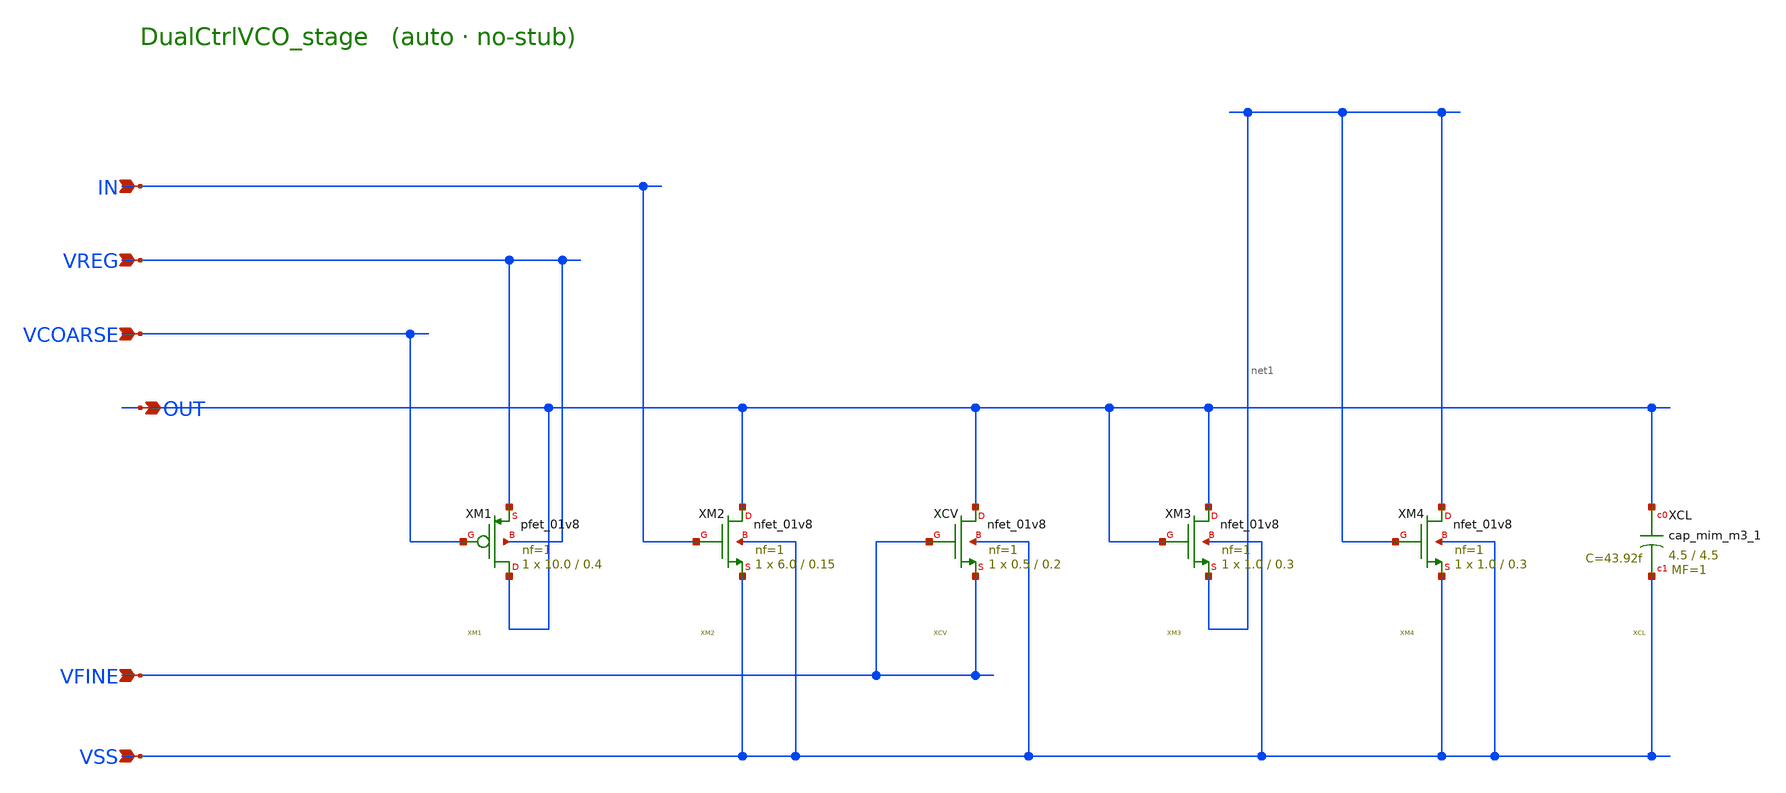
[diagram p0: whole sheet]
** sch_path: schematics/DualCtrlVCO_stage.sch
**.subckt DualCtrlVCO_stage IN OUT VCOARSE VFINE VREG VSS
*.ipin IN
*.opin OUT
*.ipin VCOARSE
*.ipin VFINE
*.ipin VREG
*.ipin VSS
XXM1 OUT VCOARSE VREG VREG sky130_fd_pr__pfet_01v8 L=0.4 W=10.0 nf=1 ad='int((nf+1)/2) * W/nf * 0.29'
+ as='int((nf+2)/2) * W/nf * 0.29' pd='2*int((nf+1)/2) * (W/nf + 0.29)' ps='2*int((nf+2)/2) * (W/nf + 0.29)'
+ nrd='0.29 / W' nrs='0.29 / W' sa=0 sb=0 sd=0 mult=1 m=1
XXM2 OUT IN VSS VSS sky130_fd_pr__nfet_01v8 L=0.15 W=6.0 nf=1 ad='int((1 + 1)/2) * 6.0 / 1 * 0.29' as='int((1 + 2)/2) * 6.0 / 1 * 0.29'
+ pd='2*int((1 + 1)/2) * (6.0 / 1 + 0.29)' ps='2*int((1 + 2)/2) * (6.0 / 1 + 0.29)' nrd='0.29 / 6.0 ' nrs='0.29 / 6.0 '
+ sa=0 sb=0 sd=0 mult=1 m=1
XXCV OUT VFINE VFINE VSS sky130_fd_pr__nfet_01v8 L=0.2 W=0.5 nf=1 ad='int((1 + 1)/2) * 0.5 / 1 * 0.29'
+ as='int((1 + 2)/2) * 0.5 / 1 * 0.29' pd='2*int((1 + 1)/2) * (0.5 / 1 + 0.29)' ps='2*int((1 + 2)/2) * (0.5 / 1 + 0.29)'
+ nrd='0.29 / 0.5 ' nrs='0.29 / 0.5 ' sa=0 sb=0 sd=0 mult=1 m=1
XXM3 OUT OUT net1 VSS sky130_fd_pr__nfet_01v8 L=0.3 W=1.0 nf=1 ad='int((1 + 1)/2) * 1.0 / 1 * 0.29' as='int((1 + 2)/2) * 1.0 / 1 * 0.29'
+ pd='2*int((1 + 1)/2) * (1.0 / 1 + 0.29)' ps='2*int((1 + 2)/2) * (1.0 / 1 + 0.29)' nrd='0.29 / 1.0 ' nrs='0.29 / 1.0 '
+ sa=0 sb=0 sd=0 mult=1 m=1
XXM4 net1 net1 VSS VSS sky130_fd_pr__nfet_01v8 L=0.3 W=1.0 nf=1 ad='int((1 + 1)/2) * 1.0 / 1 * 0.29'
+ as='int((1 + 2)/2) * 1.0 / 1 * 0.29' pd='2*int((1 + 1)/2) * (1.0 / 1 + 0.29)' ps='2*int((1 + 2)/2) * (1.0 / 1 + 0.29)'
+ nrd='0.29 / 1.0 ' nrs='0.29 / 1.0 ' sa=0 sb=0 sd=0 mult=1 m=1
XXCL OUT VSS sky130_fd_pr__cap_mim_m3_1 W=4.5 L=4.5 MF=1 m=1
**.ends
.end
